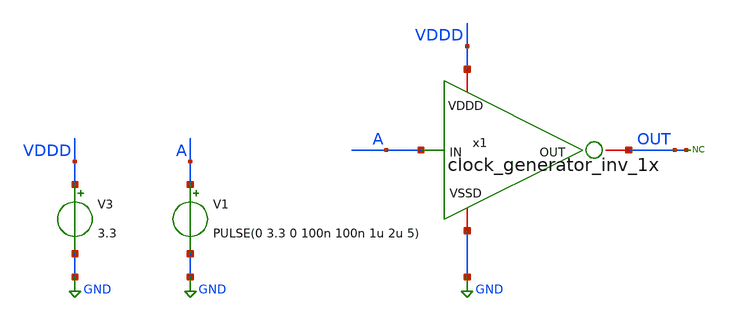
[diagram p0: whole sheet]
** sch_path: SAR_ADC/blocks/SAR_clock/clock_generator_inv_1x_tb.sch
**.subckt clock_generator_inv_1x_tb
x1 VDDD OUT GND A clock_generator_inv_1x
V1 A GND PULSE(0 3.3 0 100n 100n 1u 2u 5)
V3 VDDD GND 3.3
* noconn OUT
**** begin user architecture code



*Parameters
.options TEMPS= 27.0

*Models
.include /home/electrica/Documents/gf180_projects/pdk/gf180mcuC/libs.tech/ngspice/design.ngspice
.lib /home/electrica/Documents/gf180_projects/pdk/gf180mcuC/libs.tech/ngspice/sm141064.ngspice typical
.lib /home/electrica/Documents/gf180_projects/pdk/gf180mcuC/libs.tech/ngspice/smbb000149.ngspice typical


*Data to save
.save all

*Simulation
.control
tran 1n 30u
setplot dc1
plot V(A)+4 V(OUT)
set filetype=ascii
write clock_generator_inv_1x_tb_tran.raw

reset
unset filetype
op
save all
write clock_generator_inv_1x_tb.raw

.endc
.end



**** end user architecture code
**.ends

* expanding   symbol:
*+  /home/electrica/Documents/gf180_projects/gf180_work/PICO_contest/SAR_clock/clock_generator_inv_1x.sym # of pins=4
** sym_path: SAR_ADC/SAR_clock/xschem/clock_generator_inv_1x.sym
** sch_path: SAR_ADC/SAR_clock/xschem/clock_generator_inv_1x.sch
.subckt clock_generator_inv_1x VDDD OUT VSSD IN
*.iopin VDDD
*.iopin VSSD
*.iopin OUT
*.ipin IN
XM1 OUT IN VDDD VDDD pfet_03v3 L=0.28u W=3.9u nf=1 ad='int((nf+1)/2) * W/nf * 0.18u' as='int((nf+2)/2) * W/nf * 0.18u'
+ pd='2*int((nf+1)/2) * (W/nf + 0.18u)' ps='2*int((nf+2)/2) * (W/nf + 0.18u)' nrd='0.18u / W' nrs='0.18u / W'
+ sa=0 sb=0 sd=0 m=1
XM2 OUT IN VSSD VSSD nfet_03v3 L=0.28u W=1.56u nf=1 ad='int((nf+1)/2) * W/nf * 0.18u' as='int((nf+2)/2) * W/nf * 0.18u'
+ pd='2*int((nf+1)/2) * (W/nf + 0.18u)' ps='2*int((nf+2)/2) * (W/nf + 0.18u)' nrd='0.18u / W' nrs='0.18u / W'
+ sa=0 sb=0 sd=0 m=1
.ends

.GLOBAL GND
.end
